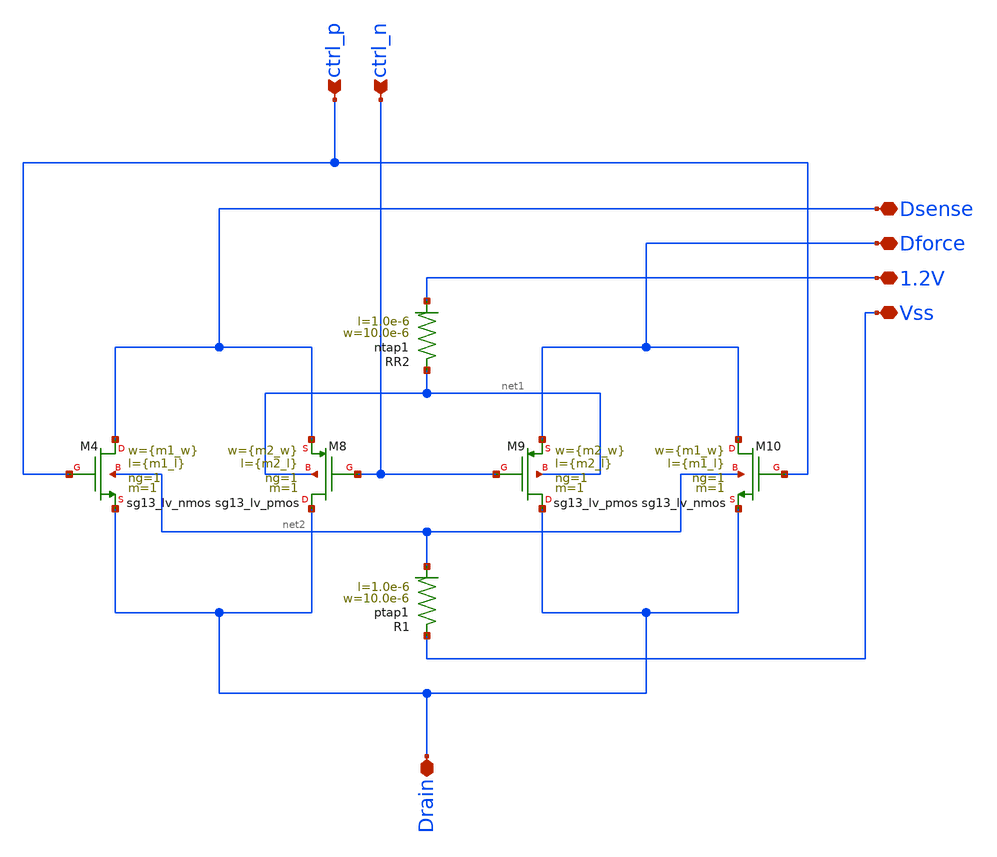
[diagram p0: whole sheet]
** sch_path: design_data/xschem/new_tb/Drain_Line.sch
**.subckt Drain_Line Vss ctrl_n 1.2V Dsense Drain Dforce ctrl_p
*.iopin Vss
*.ipin ctrl_n
*.iopin 1.2V
*.iopin Dsense
*.iopin Drain
*.iopin Dforce
*.ipin ctrl_p
XM4 Dsense ctrl_p Drain net2 sg13_lv_nmos w={m1_w} l={m1_l} ng=1 m=1 mm_ok=1
XM8 Drain ctrl_n Dsense net1 sg13_lv_pmos w={m2_w} l={m2_l} ng=1 m=1 mm_ok=1
XM9 Drain ctrl_n Dforce net1 sg13_lv_pmos w={m2_w} l={m2_l} ng=1 m=1 mm_ok=1
XM10 Dforce ctrl_p Drain net2 sg13_lv_nmos w={m1_w} l={m1_l} ng=1 m=1 mm_ok=1
XR1 Vss net2 ptap1 R=30.62 w=10.0e-6 l=1.0e-6
XR2 net1 1.2V ntap1 R=30.62 w=10.0e-6 l=1.0e-6
**.ends
.end
